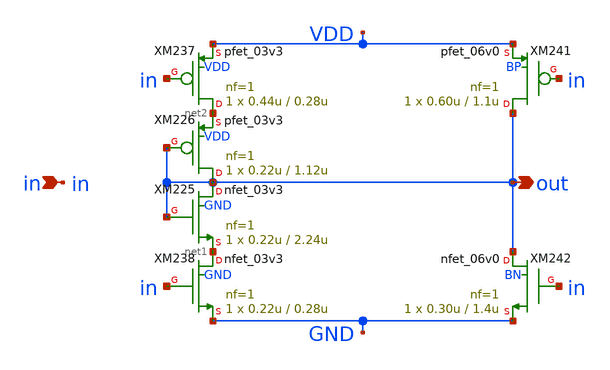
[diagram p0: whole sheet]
** sch_path: xschem_designs/STI.sch
**.subckt STI in out
*.ipin in
*.opin out
XM225 out out net1 GND nfet_03v3 L=2.24u W=0.22u nf=1 ad='int((nf+1)/2) * W/nf * 0.18u' as='int((nf+2)/2) * W/nf * 0.18u'
+ pd='2*int((nf+1)/2) * (W/nf + 0.18u)' ps='2*int((nf+2)/2) * (W/nf + 0.18u)' nrd='0.18u / W' nrs='0.18u / W'
+ sa=0 sb=0 sd=0 m=1 par=1
XM226 out out net2 VDD pfet_03v3 L=1.12u W=0.22u nf=1 ad='int((nf+1)/2) * W/nf * 0.18u' as='int((nf+2)/2) * W/nf * 0.18u'
+ pd='2*int((nf+1)/2) * (W/nf + 0.18u)' ps='2*int((nf+2)/2) * (W/nf + 0.18u)' nrd='0.18u / W' nrs='0.18u / W'
+ sa=0 sb=0 sd=0 m=1 par=1
XM237 net2 in VDD VDD pfet_03v3 L=0.28u W=0.44u nf=1 ad='int((nf+1)/2) * W/nf * 0.18u' as='int((nf+2)/2) * W/nf * 0.18u'
+ pd='2*int((nf+1)/2) * (W/nf + 0.18u)' ps='2*int((nf+2)/2) * (W/nf + 0.18u)' nrd='0.18u / W' nrs='0.18u / W'
+ sa=0 sb=0 sd=0 m=1 par=1
XM238 net1 in GND GND nfet_03v3 L=0.28u W=0.22u nf=1 ad='int((nf+1)/2) * W/nf * 0.18u' as='int((nf+2)/2) * W/nf * 0.18u'
+ pd='2*int((nf+1)/2) * (W/nf + 0.18u)' ps='2*int((nf+2)/2) * (W/nf + 0.18u)' nrd='0.18u / W' nrs='0.18u / W'
+ sa=0 sb=0 sd=0 m=1 par=1
XM241 out in VDD BP pfet_06v0 L=1.1u W=0.60u nf=1 ad='int((nf+1)/2) * W/nf * 0.18u' as='int((nf+2)/2) * W/nf * 0.18u'
+ pd='2*int((nf+1)/2) * (W/nf + 0.18u)' ps='2*int((nf+2)/2) * (W/nf + 0.18u)' nrd='0.18u / W' nrs='0.18u / W'
+ sa=0 sb=0 sd=0 m=1 par=1
XM242 out in GND BN nfet_06v0 L=1.4u W=0.30u nf=1 ad='int((nf+1)/2) * W/nf * 0.18u' as='int((nf+2)/2) * W/nf * 0.18u'
+ pd='2*int((nf+1)/2) * (W/nf + 0.18u)' ps='2*int((nf+2)/2) * (W/nf + 0.18u)' nrd='0.18u / W' nrs='0.18u / W'
+ sa=0 sb=0 sd=0 m=1 par=1
**.ends
.end
